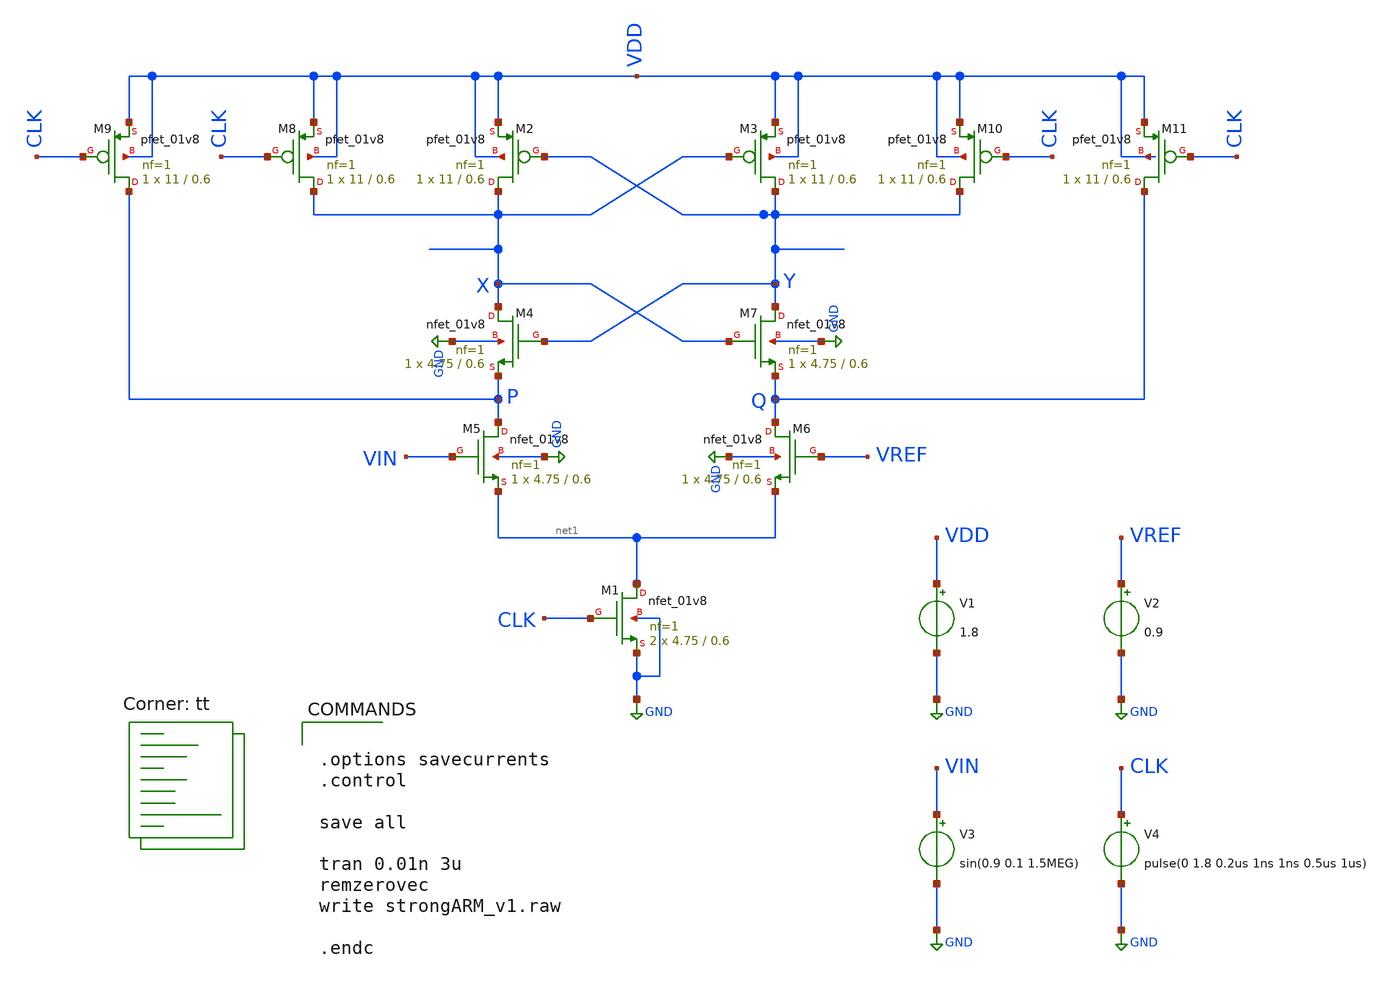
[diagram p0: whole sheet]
** sch_path: strongARM/strongARM_v1.sch
**.subckt strongARM_v1
XM1 net1 CLK GND GND sky130_fd_pr__nfet_01v8 L=0.6 W=4.75 nf=1 ad='int((nf+1)/2) * W/nf * 0.29' as='int((nf+2)/2) * W/nf * 0.29'
+ pd='2*int((nf+1)/2) * (W/nf + 0.29)' ps='2*int((nf+2)/2) * (W/nf + 0.29)' nrd='0.29 / W' nrs='0.29 / W'
+ sa=0 sb=0 sd=0 mult=2 m=2
XM2 X Y VDD VDD sky130_fd_pr__pfet_01v8 L=0.6 W=11 nf=1 ad='int((nf+1)/2) * W/nf * 0.29' as='int((nf+2)/2) * W/nf * 0.29'
+ pd='2*int((nf+1)/2) * (W/nf + 0.29)' ps='2*int((nf+2)/2) * (W/nf + 0.29)' nrd='0.29 / W' nrs='0.29 / W'
+ sa=0 sb=0 sd=0 mult=1 m=1
XM3 Y X VDD VDD sky130_fd_pr__pfet_01v8 L=0.6 W=11 nf=1 ad='int((nf+1)/2) * W/nf * 0.29' as='int((nf+2)/2) * W/nf * 0.29'
+ pd='2*int((nf+1)/2) * (W/nf + 0.29)' ps='2*int((nf+2)/2) * (W/nf + 0.29)' nrd='0.29 / W' nrs='0.29 / W'
+ sa=0 sb=0 sd=0 mult=1 m=1
XM5 P VIN net1 GND sky130_fd_pr__nfet_01v8 L=0.6 W=4.75 nf=1 ad='int((nf+1)/2) * W/nf * 0.29' as='int((nf+2)/2) * W/nf * 0.29'
+ pd='2*int((nf+1)/2) * (W/nf + 0.29)' ps='2*int((nf+2)/2) * (W/nf + 0.29)' nrd='0.29 / W' nrs='0.29 / W'
+ sa=0 sb=0 sd=0 mult=1 m=1
XM4 X Y P GND sky130_fd_pr__nfet_01v8 L=0.6 W=4.75 nf=1 ad='int((nf+1)/2) * W/nf * 0.29' as='int((nf+2)/2) * W/nf * 0.29'
+ pd='2*int((nf+1)/2) * (W/nf + 0.29)' ps='2*int((nf+2)/2) * (W/nf + 0.29)' nrd='0.29 / W' nrs='0.29 / W'
+ sa=0 sb=0 sd=0 mult=1 m=1
XM6 Q VREF net1 GND sky130_fd_pr__nfet_01v8 L=0.6 W=4.75 nf=1 ad='int((nf+1)/2) * W/nf * 0.29' as='int((nf+2)/2) * W/nf * 0.29'
+ pd='2*int((nf+1)/2) * (W/nf + 0.29)' ps='2*int((nf+2)/2) * (W/nf + 0.29)' nrd='0.29 / W' nrs='0.29 / W'
+ sa=0 sb=0 sd=0 mult=1 m=1
XM7 Y X Q GND sky130_fd_pr__nfet_01v8 L=0.6 W=4.75 nf=1 ad='int((nf+1)/2) * W/nf * 0.29' as='int((nf+2)/2) * W/nf * 0.29'
+ pd='2*int((nf+1)/2) * (W/nf + 0.29)' ps='2*int((nf+2)/2) * (W/nf + 0.29)' nrd='0.29 / W' nrs='0.29 / W'
+ sa=0 sb=0 sd=0 mult=1 m=1
XM8 X CLK VDD VDD sky130_fd_pr__pfet_01v8 L=0.6 W=11 nf=1 ad='int((nf+1)/2) * W/nf * 0.29' as='int((nf+2)/2) * W/nf * 0.29'
+ pd='2*int((nf+1)/2) * (W/nf + 0.29)' ps='2*int((nf+2)/2) * (W/nf + 0.29)' nrd='0.29 / W' nrs='0.29 / W'
+ sa=0 sb=0 sd=0 mult=1 m=1
XM9 P CLK VDD VDD sky130_fd_pr__pfet_01v8 L=0.6 W=11 nf=1 ad='int((nf+1)/2) * W/nf * 0.29' as='int((nf+2)/2) * W/nf * 0.29'
+ pd='2*int((nf+1)/2) * (W/nf + 0.29)' ps='2*int((nf+2)/2) * (W/nf + 0.29)' nrd='0.29 / W' nrs='0.29 / W'
+ sa=0 sb=0 sd=0 mult=1 m=1
XM10 Y CLK VDD VDD sky130_fd_pr__pfet_01v8 L=0.6 W=11 nf=1 ad='int((nf+1)/2) * W/nf * 0.29' as='int((nf+2)/2) * W/nf * 0.29'
+ pd='2*int((nf+1)/2) * (W/nf + 0.29)' ps='2*int((nf+2)/2) * (W/nf + 0.29)' nrd='0.29 / W' nrs='0.29 / W'
+ sa=0 sb=0 sd=0 mult=1 m=1
XM11 Q CLK VDD VDD sky130_fd_pr__pfet_01v8 L=0.6 W=11 nf=1 ad='int((nf+1)/2) * W/nf * 0.29' as='int((nf+2)/2) * W/nf * 0.29'
+ pd='2*int((nf+1)/2) * (W/nf + 0.29)' ps='2*int((nf+2)/2) * (W/nf + 0.29)' nrd='0.29 / W' nrs='0.29 / W'
+ sa=0 sb=0 sd=0 mult=1 m=1
V1 VDD GND 1.8
V3 VIN GND sin(0.9 0.1 1.5MEG)
V2 VREF GND 0.9
V4 CLK GND pulse(0 1.8 0.2us 1ns 1ns 0.5us 1us)
**** begin user architecture code
.lib $::SKYWATER_MODELS/sky130.lib.spice tt


.options savecurrents
.control

save all

tran 0.01n 3u
remzerovec
write strongARM_v1.raw

.endc


**** end user architecture code
**.ends
.GLOBAL GND
.end
